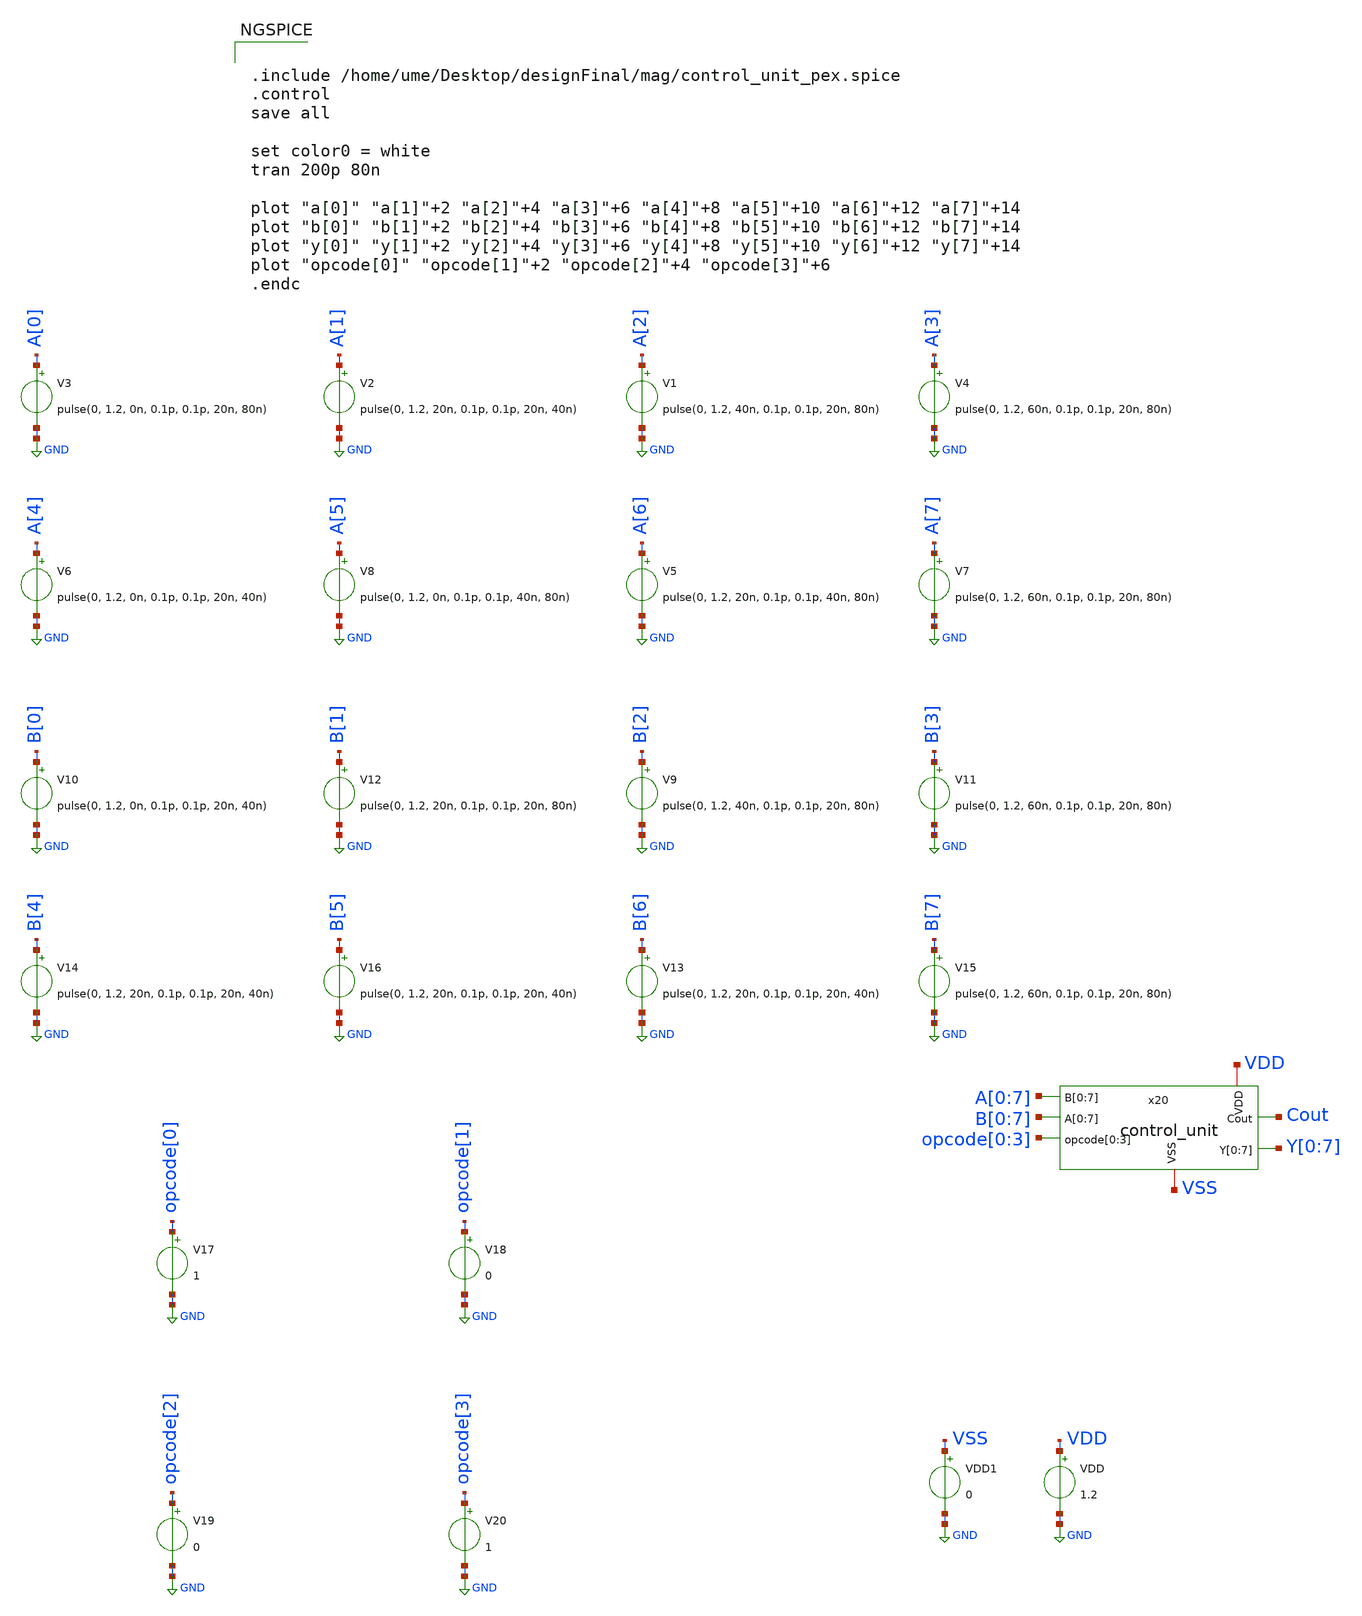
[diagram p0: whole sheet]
** sch_path: design/ALU/control_unit_tb.sch
**.subckt control_unit_tb
V17 opcode[0] GND 1
V18 opcode[1] GND 0
V1 A[2] GND pulse(0, 1.2, 40n, 0.1p, 0.1p, 20n, 80n)
V3 A[0] GND pulse(0, 1.2, 0n, 0.1p, 0.1p, 20n, 80n)
V4 A[3] GND pulse(0, 1.2, 60n, 0.1p, 0.1p, 20n, 80n)
V2 A[1] GND pulse(0, 1.2, 20n, 0.1p, 0.1p, 20n, 40n)
V5 A[6] GND pulse(0, 1.2, 20n, 0.1p, 0.1p, 40n, 80n)
V6 A[4] GND pulse(0, 1.2, 0n, 0.1p, 0.1p, 20n, 40n)
V7 A[7] GND pulse(0, 1.2, 60n, 0.1p, 0.1p, 20n, 80n)
V8 A[5] GND pulse(0, 1.2, 0n, 0.1p, 0.1p, 40n, 80n)
V9 B[2] GND pulse(0, 1.2, 40n, 0.1p, 0.1p, 20n, 80n)
V11 B[3] GND pulse(0, 1.2, 60n, 0.1p, 0.1p, 20n, 80n)
V12 B[1] GND pulse(0, 1.2, 20n, 0.1p, 0.1p, 20n, 80n)
V15 B[7] GND pulse(0, 1.2, 60n, 0.1p, 0.1p, 20n, 80n)
V10 B[0] GND pulse(0, 1.2, 0n, 0.1p, 0.1p, 20n, 40n)
V16 B[5] GND pulse(0, 1.2, 20n, 0.1p, 0.1p, 20n, 40n)
V14 B[4] GND pulse(0, 1.2, 20n, 0.1p, 0.1p, 20n, 40n)
V13 B[6] GND pulse(0, 1.2, 20n, 0.1p, 0.1p, 20n, 40n)
V19 opcode[2] GND 0
V20 opcode[3] GND 1
VDD VDD GND 1.2
VDD1 VSS GND 0
x20 A[0] A[1] A[2] A[3] A[4] A[5] A[6] A[7] B[0] B[1] B[2] B[3] B[4] B[5] B[6] B[7] Y[0] Y[1] Y[2]
+ Y[3] Y[4] Y[5] Y[6] Y[7] VDD VSS opcode[0] opcode[1] opcode[2] opcode[3] Cout control_unit
**** begin user architecture code


.include /home/ume/Desktop/designFinal/mag/control_unit_pex.spice
.control
save all

set color0 = white
tran 200p 80n

plot "a[0]" "a[1]"+2 "a[2]"+4 "a[3]"+6 "a[4]"+8 "a[5]"+10 "a[6]"+12 "a[7]"+14
plot "b[0]" "b[1]"+2 "b[2]"+4 "b[3]"+6 "b[4]"+8 "b[5]"+10 "b[6]"+12 "b[7]"+14
plot "y[0]" "y[1]"+2 "y[2]"+4 "y[3]"+6 "y[4]"+8 "y[5]"+10 "y[6]"+12 "y[7]"+14
plot "opcode[0]" "opcode[1]"+2 "opcode[2]"+4 "opcode[3]"+6
.endc


** opencircuitdesign pdks install
.lib $::SKYWATER_MODELS/sky130.lib.spice tt_mm


**** end user architecture code
**.ends
.GLOBAL GND
.end
